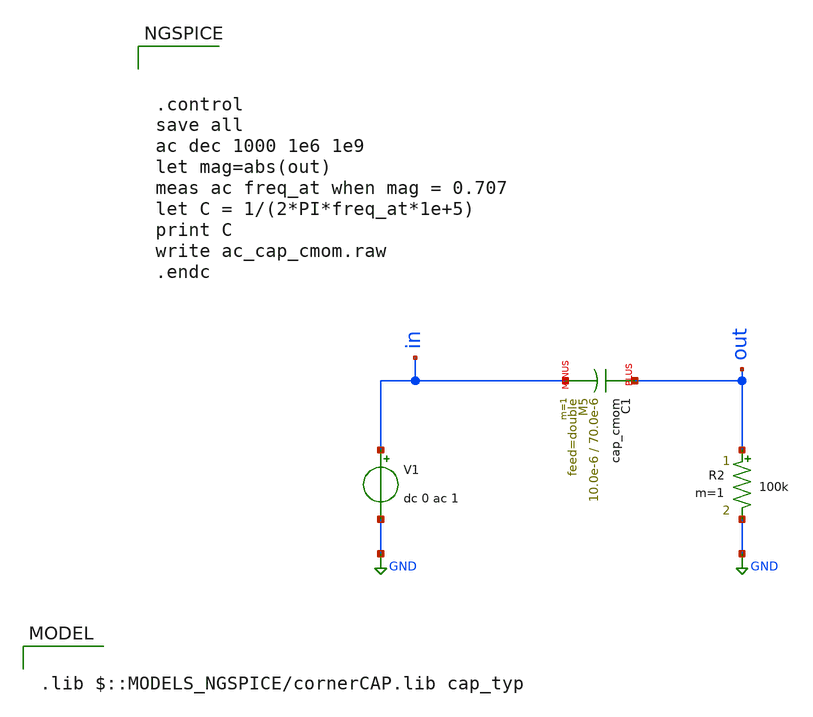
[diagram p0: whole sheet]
** sch_path: ihp-sg13g2/libs.tech/xschem/sg13g2_tests/ac_cap_cmom.sch
* Copyright 2021 Stefan Frederik Schippers
* Licensed under the Apache License, Version 2.0 (the "License");
* you may not use this file except in compliance with the License.
* You may obtain a copy of the License at
* https://www.apache.org/licenses/LICENSE-2.0
* Unless required by applicable law or agreed to in writing, software
* distributed under the License is distributed on an "AS IS" BASIS,
* WITHOUT WARRANTIES OR CONDITIONS OF ANY KIND, either express or implied.
* See the License for the specific language governing permissions and
* limitations under the License.
* Copyright 2026 IHP PDK Authors
**.subckt ac_cap_cmom
V1 in GND dc 0 ac 1
R2 out GND 100k m=1
XC1 out in cap_cmom w=10.0e-6 l=70.0e-6 mmin=1 mmax=5 feed=double subblock=0 m=1 mm_ok=1
**** begin user architecture code



.control
save all
ac dec 1000 1e6 1e9
let mag=abs(out)
meas ac freq_at when mag = 0.707
let C = 1/(2*PI*freq_at*1e+5)
print C
write ac_cap_cmom.raw
.endc



.lib $::MODELS_NGSPICE/cornerCAP.lib cap_typ

**** end user architecture code
**.ends
.GLOBAL GND
.end
